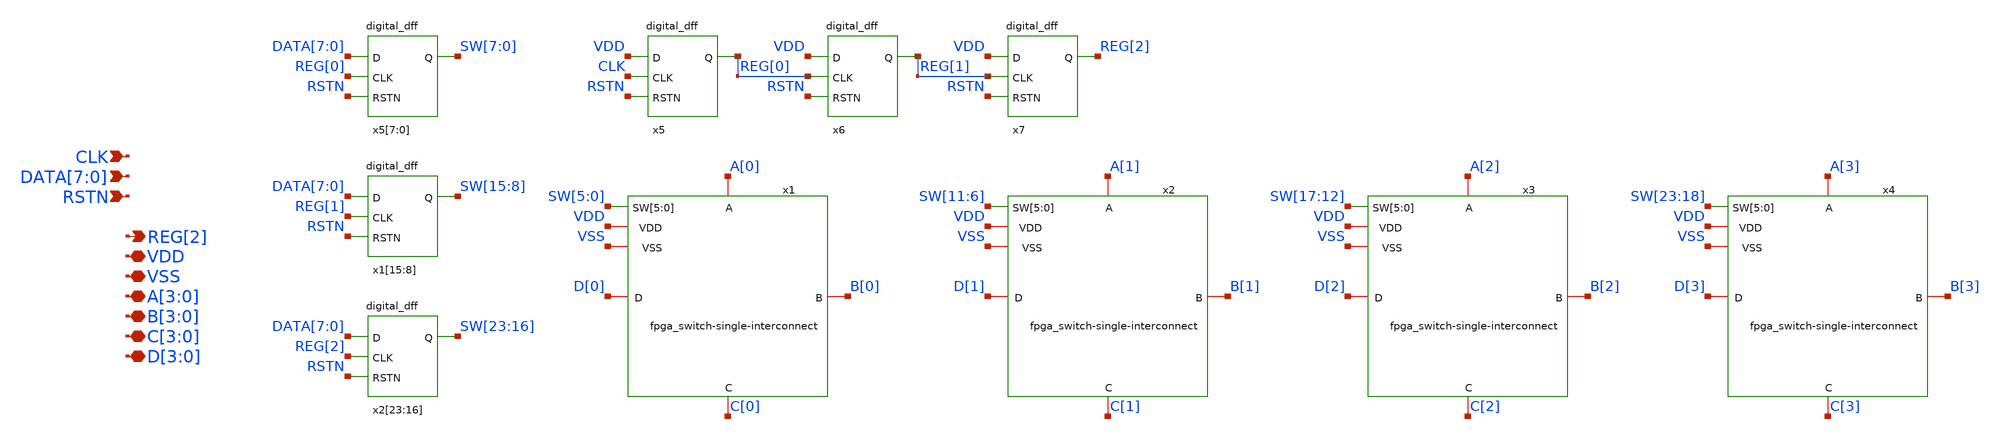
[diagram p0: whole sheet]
** sch_path: designs/libs/core_analog/fpga_switch/fpga_switch-interconnect-block.sch
**.subckt fpga_switch-interconnect-block VDD VSS
*+ DATA[7],DATA[6],DATA[5],DATA[4],DATA[3],DATA[2],DATA[1],DATA[0] CLK A[3],A[2],A[1],A[0] B[3],B[2],B[1],B[0] C[3],C[2],C[1],C[0] D[3],D[2],D[1],D[0] RSTN REG[2]
*.iopin VDD
*.iopin VSS
*.ipin DATA[7],DATA[6],DATA[5],DATA[4],DATA[3],DATA[2],DATA[1],DATA[0]
*.ipin CLK
*.iopin A[3],A[2],A[1],A[0]
*.iopin B[3],B[2],B[1],B[0]
*.iopin C[3],C[2],C[1],C[0]
*.iopin D[3],D[2],D[1],D[0]
*.ipin RSTN
*.opin REG[2]
x1 SW[5] SW[4] SW[3] SW[2] SW[1] SW[0] VDD VSS A[0] B[0] C[0] D[0] fpga_switch-single-interconnect
x2 SW[11] SW[10] SW[9] SW[8] SW[7] SW[6] VDD VSS A[1] B[1] C[1] D[1] fpga_switch-single-interconnect
x3 SW[17] SW[16] SW[15] SW[14] SW[13] SW[12] VDD VSS A[2] B[2] C[2] D[2]
+ fpga_switch-single-interconnect
x4 SW[23] SW[22] SW[21] SW[20] SW[19] SW[18] VDD VSS A[3] B[3] C[3] D[3]
+ fpga_switch-single-interconnect
x5[7] DATA[7] REG[0] RSTN VSS VDD SW[7] digital_dff
x5[6] DATA[6] REG[0] RSTN VSS VDD SW[6] digital_dff
x5[5] DATA[5] REG[0] RSTN VSS VDD SW[5] digital_dff
x5[4] DATA[4] REG[0] RSTN VSS VDD SW[4] digital_dff
x5[3] DATA[3] REG[0] RSTN VSS VDD SW[3] digital_dff
x5[2] DATA[2] REG[0] RSTN VSS VDD SW[2] digital_dff
x5[1] DATA[1] REG[0] RSTN VSS VDD SW[1] digital_dff
x5[0] DATA[0] REG[0] RSTN VSS VDD SW[0] digital_dff
x1[15] DATA[7] REG[1] RSTN VSS VDD SW[15] digital_dff
x1[14] DATA[6] REG[1] RSTN VSS VDD SW[14] digital_dff
x1[13] DATA[5] REG[1] RSTN VSS VDD SW[13] digital_dff
x1[12] DATA[4] REG[1] RSTN VSS VDD SW[12] digital_dff
x1[11] DATA[3] REG[1] RSTN VSS VDD SW[11] digital_dff
x1[10] DATA[2] REG[1] RSTN VSS VDD SW[10] digital_dff
x1[9] DATA[1] REG[1] RSTN VSS VDD SW[9] digital_dff
x1[8] DATA[0] REG[1] RSTN VSS VDD SW[8] digital_dff
x2[23] DATA[7] REG[2] RSTN VSS VDD SW[23] digital_dff
x2[22] DATA[6] REG[2] RSTN VSS VDD SW[22] digital_dff
x2[21] DATA[5] REG[2] RSTN VSS VDD SW[21] digital_dff
x2[20] DATA[4] REG[2] RSTN VSS VDD SW[20] digital_dff
x2[19] DATA[3] REG[2] RSTN VSS VDD SW[19] digital_dff
x2[18] DATA[2] REG[2] RSTN VSS VDD SW[18] digital_dff
x2[17] DATA[1] REG[2] RSTN VSS VDD SW[17] digital_dff
x2[16] DATA[0] REG[2] RSTN VSS VDD SW[16] digital_dff
x5 VDD CLK RSTN VSS VDD REG[0] digital_dff
x6 VDD REG[0] RSTN VSS VDD REG[1] digital_dff
x7 VDD REG[1] RSTN VSS VDD REG[2] digital_dff
**.ends
.end
